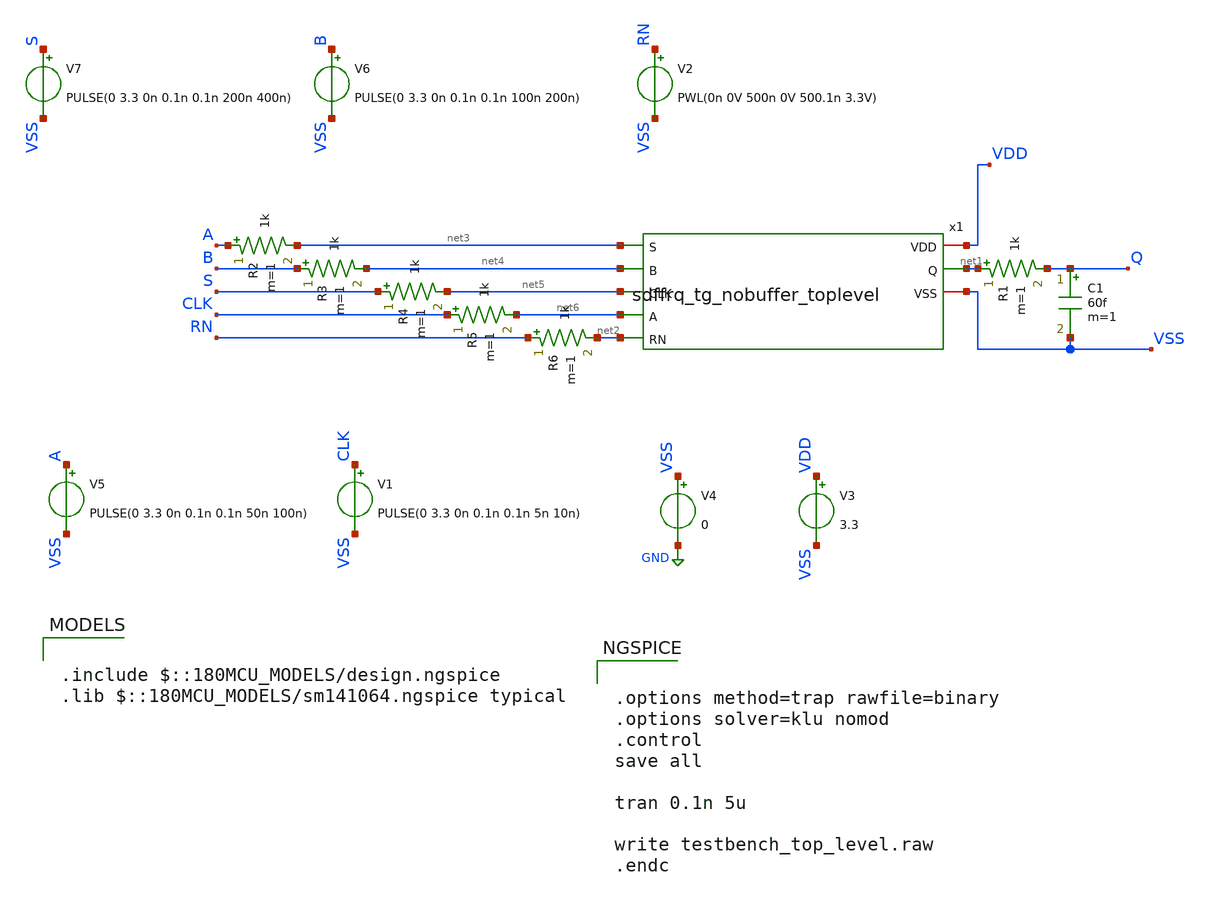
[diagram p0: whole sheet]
** sch_path: designs/libs/tb_digital/tb_toplevel/testbench_sdffrq_mux_tg.sch
**.subckt testbench_sdffrq_mux_tg
V1 CLK VSS PULSE(0 3.3 0n 0.1n 0.1n 5n 10n)
V3 VDD VSS 3.3
V4 VSS GND 0
V5 A VSS PULSE(0 3.3 0n 0.1n 0.1n 50n 100n)
V6 B VSS PULSE(0 3.3 0n 0.1n 0.1n 100n 200n)
V7 S VSS PULSE(0 3.3 0n 0.1n 0.1n 200n 400n)
V2 RN VSS PWL(0n 0V 500n 0V 500.1n 3.3V)
x1 net3 VDD net1 net4 net5 net6 net2 VSS sdffrq_tg_nobuffer_toplevel
R1 net1 Q 1k m=1
C1 Q VSS 60f m=1
R2 A net3 1k m=1
R3 B net4 1k m=1
R4 S net5 1k m=1
R5 CLK net6 1k m=1
R6 RN net2 1k m=1
**** begin user architecture code

.include $::180MCU_MODELS/design.ngspice
.lib $::180MCU_MODELS/sm141064.ngspice typical



.options method=trap rawfile=binary
.options solver=klu nomod
.control
save all

tran 0.1n 5u

write testbench_top_level.raw
.endc


**** end user architecture code
**.ends
.GLOBAL GND
.end
